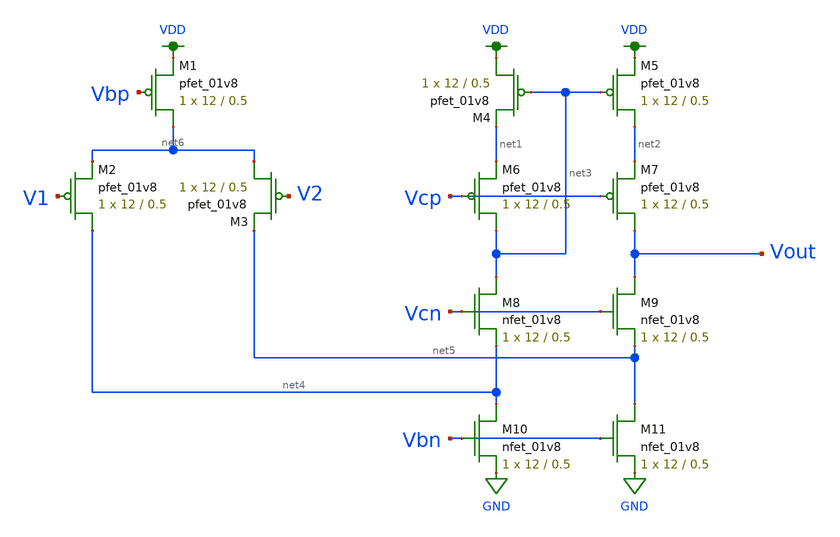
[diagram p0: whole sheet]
** sch_path: schematic/test_folded_cascode.sch
**.subckt test_folded_cascode
XM1 net6 Vbp VDD VDD sky130_fd_pr__pfet_01v8 L=0.5 W=12 nf=1 ad='int((nf+1)/2) * W/nf * 0.29' as='int((nf+2)/2) * W/nf * 0.29'
+ pd='2*int((nf+1)/2) * (W/nf + 0.29)' ps='2*int((nf+2)/2) * (W/nf + 0.29)' nrd='0.29 / W' nrs='0.29 / W'
+ sa=0 sb=0 sd=0 mult=1 m=1
XM2 net4 V1 net6 VDD sky130_fd_pr__pfet_01v8 L=0.5 W=12 nf=1 ad='int((nf+1)/2) * W/nf * 0.29' as='int((nf+2)/2) * W/nf * 0.29'
+ pd='2*int((nf+1)/2) * (W/nf + 0.29)' ps='2*int((nf+2)/2) * (W/nf + 0.29)' nrd='0.29 / W' nrs='0.29 / W'
+ sa=0 sb=0 sd=0 mult=1 m=1
XM3 net6 V2 net5 VDD sky130_fd_pr__pfet_01v8 L=0.5 W=12 nf=1 ad='int((nf+1)/2) * W/nf * 0.29' as='int((nf+2)/2) * W/nf * 0.29'
+ pd='2*int((nf+1)/2) * (W/nf + 0.29)' ps='2*int((nf+2)/2) * (W/nf + 0.29)' nrd='0.29 / W' nrs='0.29 / W'
+ sa=0 sb=0 sd=0 mult=1 m=1
XM4 VDD net3 net1 VDD sky130_fd_pr__pfet_01v8 L=0.5 W=12 nf=1 ad='int((nf+1)/2) * W/nf * 0.29' as='int((nf+2)/2) * W/nf * 0.29'
+ pd='2*int((nf+1)/2) * (W/nf + 0.29)' ps='2*int((nf+2)/2) * (W/nf + 0.29)' nrd='0.29 / W' nrs='0.29 / W'
+ sa=0 sb=0 sd=0 mult=1 m=1
XM5 net2 net3 VDD VDD sky130_fd_pr__pfet_01v8 L=0.5 W=12 nf=1 ad='int((nf+1)/2) * W/nf * 0.29' as='int((nf+2)/2) * W/nf * 0.29'
+ pd='2*int((nf+1)/2) * (W/nf + 0.29)' ps='2*int((nf+2)/2) * (W/nf + 0.29)' nrd='0.29 / W' nrs='0.29 / W'
+ sa=0 sb=0 sd=0 mult=1 m=1
XM6 net3 Vcp net1 VDD sky130_fd_pr__pfet_01v8 L=0.5 W=12 nf=1 ad='int((nf+1)/2) * W/nf * 0.29' as='int((nf+2)/2) * W/nf * 0.29'
+ pd='2*int((nf+1)/2) * (W/nf + 0.29)' ps='2*int((nf+2)/2) * (W/nf + 0.29)' nrd='0.29 / W' nrs='0.29 / W'
+ sa=0 sb=0 sd=0 mult=1 m=1
XM7 Vout Vcp net2 VDD sky130_fd_pr__pfet_01v8 L=0.5 W=12 nf=1 ad='int((nf+1)/2) * W/nf * 0.29' as='int((nf+2)/2) * W/nf * 0.29'
+ pd='2*int((nf+1)/2) * (W/nf + 0.29)' ps='2*int((nf+2)/2) * (W/nf + 0.29)' nrd='0.29 / W' nrs='0.29 / W'
+ sa=0 sb=0 sd=0 mult=1 m=1
XM8 net3 Vcn net4 GND sky130_fd_pr__nfet_01v8 L=0.5 W=12 nf=1 ad='int((nf+1)/2) * W/nf * 0.29' as='int((nf+2)/2) * W/nf * 0.29'
+ pd='2*int((nf+1)/2) * (W/nf + 0.29)' ps='2*int((nf+2)/2) * (W/nf + 0.29)' nrd='0.29 / W' nrs='0.29 / W'
+ sa=0 sb=0 sd=0 mult=1 m=1
XM9 Vout Vcn net5 GND sky130_fd_pr__nfet_01v8 L=0.5 W=12 nf=1 ad='int((nf+1)/2) * W/nf * 0.29' as='int((nf+2)/2) * W/nf * 0.29'
+ pd='2*int((nf+1)/2) * (W/nf + 0.29)' ps='2*int((nf+2)/2) * (W/nf + 0.29)' nrd='0.29 / W' nrs='0.29 / W'
+ sa=0 sb=0 sd=0 mult=1 m=1
XM10 net4 Vbn GND GND sky130_fd_pr__nfet_01v8 L=0.5 W=12 nf=1 ad='int((nf+1)/2) * W/nf * 0.29' as='int((nf+2)/2) * W/nf * 0.29'
+ pd='2*int((nf+1)/2) * (W/nf + 0.29)' ps='2*int((nf+2)/2) * (W/nf + 0.29)' nrd='0.29 / W' nrs='0.29 / W'
+ sa=0 sb=0 sd=0 mult=1 m=1
XM11 net5 Vbn GND GND sky130_fd_pr__nfet_01v8 L=0.5 W=12 nf=1 ad='int((nf+1)/2) * W/nf * 0.29' as='int((nf+2)/2) * W/nf * 0.29'
+ pd='2*int((nf+1)/2) * (W/nf + 0.29)' ps='2*int((nf+2)/2) * (W/nf + 0.29)' nrd='0.29 / W' nrs='0.29 / W'
+ sa=0 sb=0 sd=0 mult=1 m=1
**.ends
.GLOBAL VDD
.GLOBAL GND
.end
